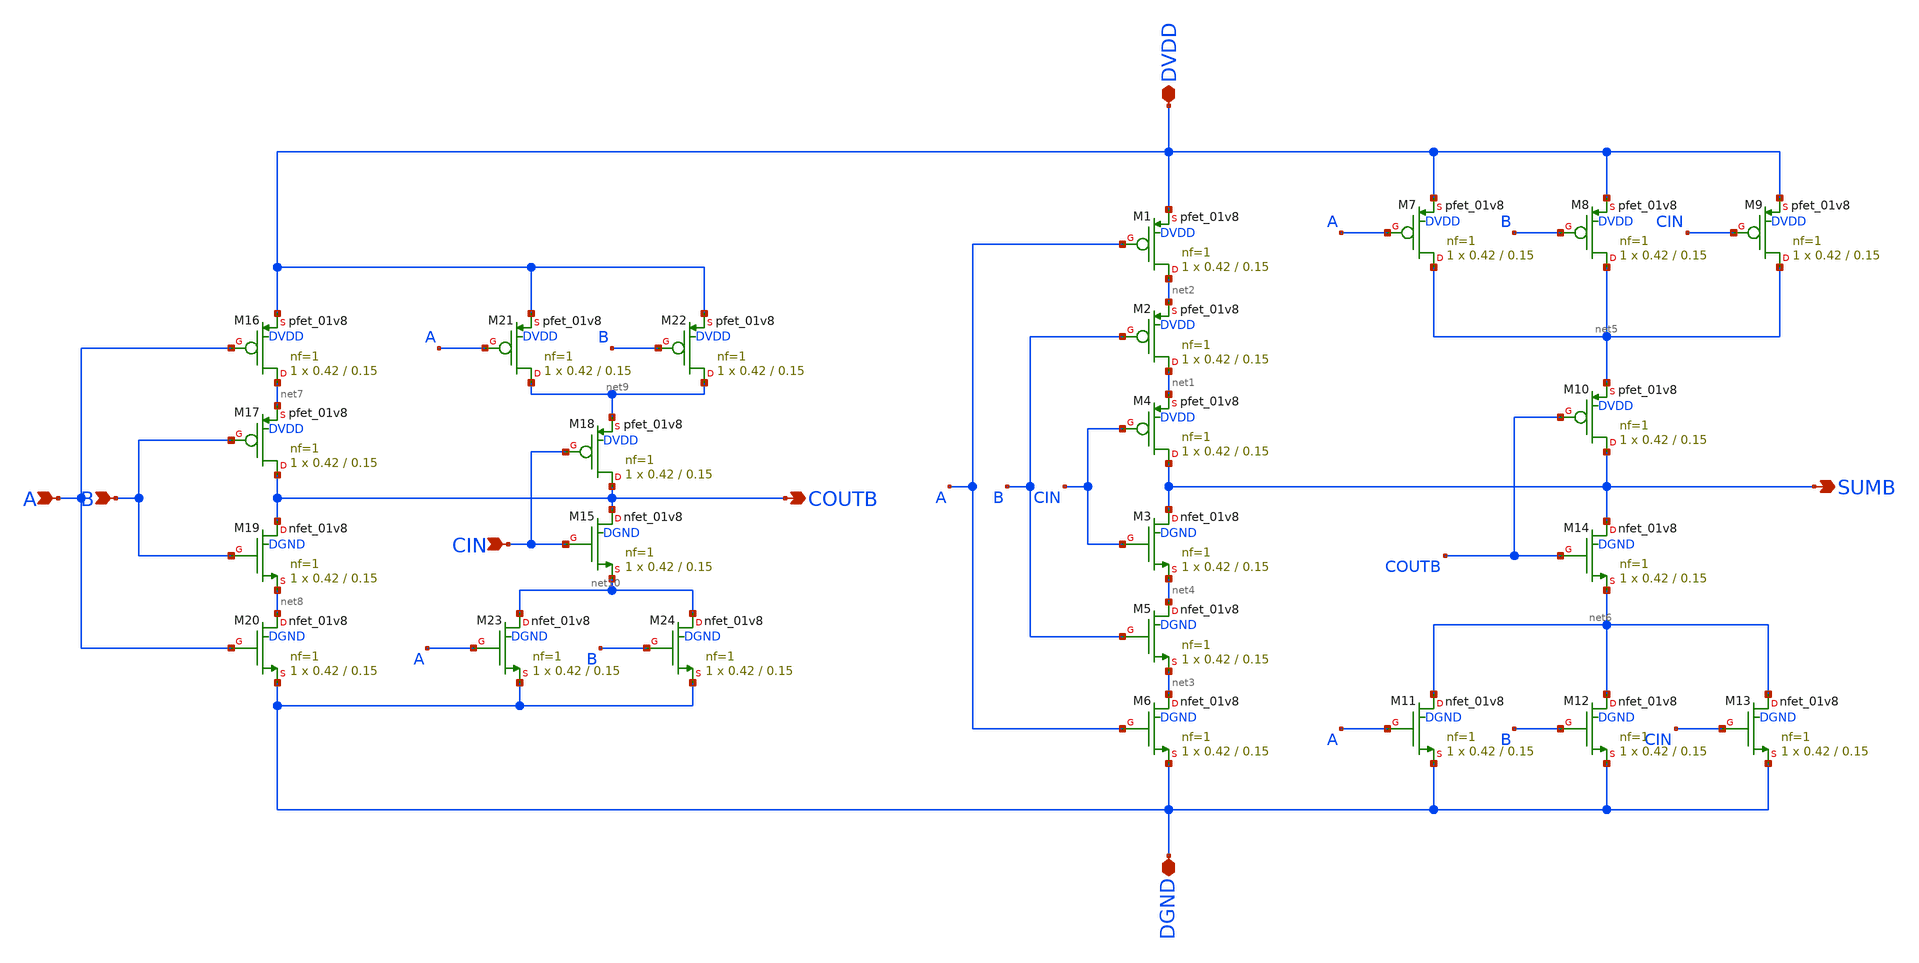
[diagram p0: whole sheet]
** sch_path: project/sch_sym_files/fa.sch
**.subckt fa COUTB CIN DVDD DGND SUMB B A
*.opin COUTB
*.ipin CIN
*.iopin DVDD
*.iopin DGND
*.opin SUMB
*.ipin B
*.ipin A
XM3 SUMB CIN net4 DGND sky130_fd_pr__nfet_01v8 L=0.15 W=0.42 nf=1 ad='int((nf+1)/2) * W/nf * 0.29' as='int((nf+2)/2) * W/nf * 0.29'
+ pd='2*int((nf+1)/2) * (W/nf + 0.29)' ps='2*int((nf+2)/2) * (W/nf + 0.29)' nrd='0.29 / W' nrs='0.29 / W'
+ sa=0 sb=0 sd=0 mult=1 m=1
XM1 net2 A DVDD DVDD sky130_fd_pr__pfet_01v8 L=0.15 W=0.42 nf=1 ad='int((nf+1)/2) * W/nf * 0.29' as='int((nf+2)/2) * W/nf * 0.29'
+ pd='2*int((nf+1)/2) * (W/nf + 0.29)' ps='2*int((nf+2)/2) * (W/nf + 0.29)' nrd='0.29 / W' nrs='0.29 / W'
+ sa=0 sb=0 sd=0 mult=1 m=1
XM2 net1 B net2 DVDD sky130_fd_pr__pfet_01v8 L=0.15 W=0.42 nf=1 ad='int((nf+1)/2) * W/nf * 0.29' as='int((nf+2)/2) * W/nf * 0.29'
+ pd='2*int((nf+1)/2) * (W/nf + 0.29)' ps='2*int((nf+2)/2) * (W/nf + 0.29)' nrd='0.29 / W' nrs='0.29 / W'
+ sa=0 sb=0 sd=0 mult=1 m=1
XM4 SUMB CIN net1 DVDD sky130_fd_pr__pfet_01v8 L=0.15 W=0.42 nf=1 ad='int((nf+1)/2) * W/nf * 0.29' as='int((nf+2)/2) * W/nf * 0.29'
+ pd='2*int((nf+1)/2) * (W/nf + 0.29)' ps='2*int((nf+2)/2) * (W/nf + 0.29)' nrd='0.29 / W' nrs='0.29 / W'
+ sa=0 sb=0 sd=0 mult=1 m=1
XM5 net4 B net3 DGND sky130_fd_pr__nfet_01v8 L=0.15 W=0.42 nf=1 ad='int((nf+1)/2) * W/nf * 0.29' as='int((nf+2)/2) * W/nf * 0.29'
+ pd='2*int((nf+1)/2) * (W/nf + 0.29)' ps='2*int((nf+2)/2) * (W/nf + 0.29)' nrd='0.29 / W' nrs='0.29 / W'
+ sa=0 sb=0 sd=0 mult=1 m=1
XM6 net3 A DGND DGND sky130_fd_pr__nfet_01v8 L=0.15 W=0.42 nf=1 ad='int((nf+1)/2) * W/nf * 0.29' as='int((nf+2)/2) * W/nf * 0.29'
+ pd='2*int((nf+1)/2) * (W/nf + 0.29)' ps='2*int((nf+2)/2) * (W/nf + 0.29)' nrd='0.29 / W' nrs='0.29 / W'
+ sa=0 sb=0 sd=0 mult=1 m=1
XM7 net5 A DVDD DVDD sky130_fd_pr__pfet_01v8 L=0.15 W=0.42 nf=1 ad='int((nf+1)/2) * W/nf * 0.29' as='int((nf+2)/2) * W/nf * 0.29'
+ pd='2*int((nf+1)/2) * (W/nf + 0.29)' ps='2*int((nf+2)/2) * (W/nf + 0.29)' nrd='0.29 / W' nrs='0.29 / W'
+ sa=0 sb=0 sd=0 mult=1 m=1
XM8 net5 B DVDD DVDD sky130_fd_pr__pfet_01v8 L=0.15 W=0.42 nf=1 ad='int((nf+1)/2) * W/nf * 0.29' as='int((nf+2)/2) * W/nf * 0.29'
+ pd='2*int((nf+1)/2) * (W/nf + 0.29)' ps='2*int((nf+2)/2) * (W/nf + 0.29)' nrd='0.29 / W' nrs='0.29 / W'
+ sa=0 sb=0 sd=0 mult=1 m=1
XM9 net5 CIN DVDD DVDD sky130_fd_pr__pfet_01v8 L=0.15 W=0.42 nf=1 ad='int((nf+1)/2) * W/nf * 0.29' as='int((nf+2)/2) * W/nf * 0.29'
+ pd='2*int((nf+1)/2) * (W/nf + 0.29)' ps='2*int((nf+2)/2) * (W/nf + 0.29)' nrd='0.29 / W' nrs='0.29 / W'
+ sa=0 sb=0 sd=0 mult=1 m=1
XM10 SUMB COUTB net5 DVDD sky130_fd_pr__pfet_01v8 L=0.15 W=0.42 nf=1 ad='int((nf+1)/2) * W/nf * 0.29'
+ as='int((nf+2)/2) * W/nf * 0.29' pd='2*int((nf+1)/2) * (W/nf + 0.29)' ps='2*int((nf+2)/2) * (W/nf + 0.29)'
+ nrd='0.29 / W' nrs='0.29 / W' sa=0 sb=0 sd=0 mult=1 m=1
XM11 net6 A DGND DGND sky130_fd_pr__nfet_01v8 L=0.15 W=0.42 nf=1 ad='int((nf+1)/2) * W/nf * 0.29' as='int((nf+2)/2) * W/nf * 0.29'
+ pd='2*int((nf+1)/2) * (W/nf + 0.29)' ps='2*int((nf+2)/2) * (W/nf + 0.29)' nrd='0.29 / W' nrs='0.29 / W'
+ sa=0 sb=0 sd=0 mult=1 m=1
XM12 net6 B DGND DGND sky130_fd_pr__nfet_01v8 L=0.15 W=0.42 nf=1 ad='int((nf+1)/2) * W/nf * 0.29' as='int((nf+2)/2) * W/nf * 0.29'
+ pd='2*int((nf+1)/2) * (W/nf + 0.29)' ps='2*int((nf+2)/2) * (W/nf + 0.29)' nrd='0.29 / W' nrs='0.29 / W'
+ sa=0 sb=0 sd=0 mult=1 m=1
XM13 net6 CIN DGND DGND sky130_fd_pr__nfet_01v8 L=0.15 W=0.42 nf=1 ad='int((nf+1)/2) * W/nf * 0.29' as='int((nf+2)/2) * W/nf * 0.29'
+ pd='2*int((nf+1)/2) * (W/nf + 0.29)' ps='2*int((nf+2)/2) * (W/nf + 0.29)' nrd='0.29 / W' nrs='0.29 / W'
+ sa=0 sb=0 sd=0 mult=1 m=1
XM14 SUMB COUTB net6 DGND sky130_fd_pr__nfet_01v8 L=0.15 W=0.42 nf=1 ad='int((nf+1)/2) * W/nf * 0.29'
+ as='int((nf+2)/2) * W/nf * 0.29' pd='2*int((nf+1)/2) * (W/nf + 0.29)' ps='2*int((nf+2)/2) * (W/nf + 0.29)'
+ nrd='0.29 / W' nrs='0.29 / W' sa=0 sb=0 sd=0 mult=1 m=1
XM15 COUTB CIN net10 DGND sky130_fd_pr__nfet_01v8 L=0.15 W=0.42 nf=1 ad='int((nf+1)/2) * W/nf * 0.29'
+ as='int((nf+2)/2) * W/nf * 0.29' pd='2*int((nf+1)/2) * (W/nf + 0.29)' ps='2*int((nf+2)/2) * (W/nf + 0.29)'
+ nrd='0.29 / W' nrs='0.29 / W' sa=0 sb=0 sd=0 mult=1 m=1
XM16 net7 A DVDD DVDD sky130_fd_pr__pfet_01v8 L=0.15 W=0.42 nf=1 ad='int((nf+1)/2) * W/nf * 0.29' as='int((nf+2)/2) * W/nf * 0.29'
+ pd='2*int((nf+1)/2) * (W/nf + 0.29)' ps='2*int((nf+2)/2) * (W/nf + 0.29)' nrd='0.29 / W' nrs='0.29 / W'
+ sa=0 sb=0 sd=0 mult=1 m=1
XM17 COUTB B net7 DVDD sky130_fd_pr__pfet_01v8 L=0.15 W=0.42 nf=1 ad='int((nf+1)/2) * W/nf * 0.29' as='int((nf+2)/2) * W/nf * 0.29'
+ pd='2*int((nf+1)/2) * (W/nf + 0.29)' ps='2*int((nf+2)/2) * (W/nf + 0.29)' nrd='0.29 / W' nrs='0.29 / W'
+ sa=0 sb=0 sd=0 mult=1 m=1
XM18 COUTB CIN net9 DVDD sky130_fd_pr__pfet_01v8 L=0.15 W=0.42 nf=1 ad='int((nf+1)/2) * W/nf * 0.29'
+ as='int((nf+2)/2) * W/nf * 0.29' pd='2*int((nf+1)/2) * (W/nf + 0.29)' ps='2*int((nf+2)/2) * (W/nf + 0.29)'
+ nrd='0.29 / W' nrs='0.29 / W' sa=0 sb=0 sd=0 mult=1 m=1
XM19 COUTB B net8 DGND sky130_fd_pr__nfet_01v8 L=0.15 W=0.42 nf=1 ad='int((nf+1)/2) * W/nf * 0.29' as='int((nf+2)/2) * W/nf * 0.29'
+ pd='2*int((nf+1)/2) * (W/nf + 0.29)' ps='2*int((nf+2)/2) * (W/nf + 0.29)' nrd='0.29 / W' nrs='0.29 / W'
+ sa=0 sb=0 sd=0 mult=1 m=1
XM20 net8 A DGND DGND sky130_fd_pr__nfet_01v8 L=0.15 W=0.42 nf=1 ad='int((nf+1)/2) * W/nf * 0.29' as='int((nf+2)/2) * W/nf * 0.29'
+ pd='2*int((nf+1)/2) * (W/nf + 0.29)' ps='2*int((nf+2)/2) * (W/nf + 0.29)' nrd='0.29 / W' nrs='0.29 / W'
+ sa=0 sb=0 sd=0 mult=1 m=1
XM21 net9 A DVDD DVDD sky130_fd_pr__pfet_01v8 L=0.15 W=0.42 nf=1 ad='int((nf+1)/2) * W/nf * 0.29' as='int((nf+2)/2) * W/nf * 0.29'
+ pd='2*int((nf+1)/2) * (W/nf + 0.29)' ps='2*int((nf+2)/2) * (W/nf + 0.29)' nrd='0.29 / W' nrs='0.29 / W'
+ sa=0 sb=0 sd=0 mult=1 m=1
XM22 net9 B DVDD DVDD sky130_fd_pr__pfet_01v8 L=0.15 W=0.42 nf=1 ad='int((nf+1)/2) * W/nf * 0.29' as='int((nf+2)/2) * W/nf * 0.29'
+ pd='2*int((nf+1)/2) * (W/nf + 0.29)' ps='2*int((nf+2)/2) * (W/nf + 0.29)' nrd='0.29 / W' nrs='0.29 / W'
+ sa=0 sb=0 sd=0 mult=1 m=1
XM23 net10 A DGND DGND sky130_fd_pr__nfet_01v8 L=0.15 W=0.42 nf=1 ad='int((nf+1)/2) * W/nf * 0.29' as='int((nf+2)/2) * W/nf * 0.29'
+ pd='2*int((nf+1)/2) * (W/nf + 0.29)' ps='2*int((nf+2)/2) * (W/nf + 0.29)' nrd='0.29 / W' nrs='0.29 / W'
+ sa=0 sb=0 sd=0 mult=1 m=1
XM24 net10 B DGND DGND sky130_fd_pr__nfet_01v8 L=0.15 W=0.42 nf=1 ad='int((nf+1)/2) * W/nf * 0.29' as='int((nf+2)/2) * W/nf * 0.29'
+ pd='2*int((nf+1)/2) * (W/nf + 0.29)' ps='2*int((nf+2)/2) * (W/nf + 0.29)' nrd='0.29 / W' nrs='0.29 / W'
+ sa=0 sb=0 sd=0 mult=1 m=1
**.ends
.end
